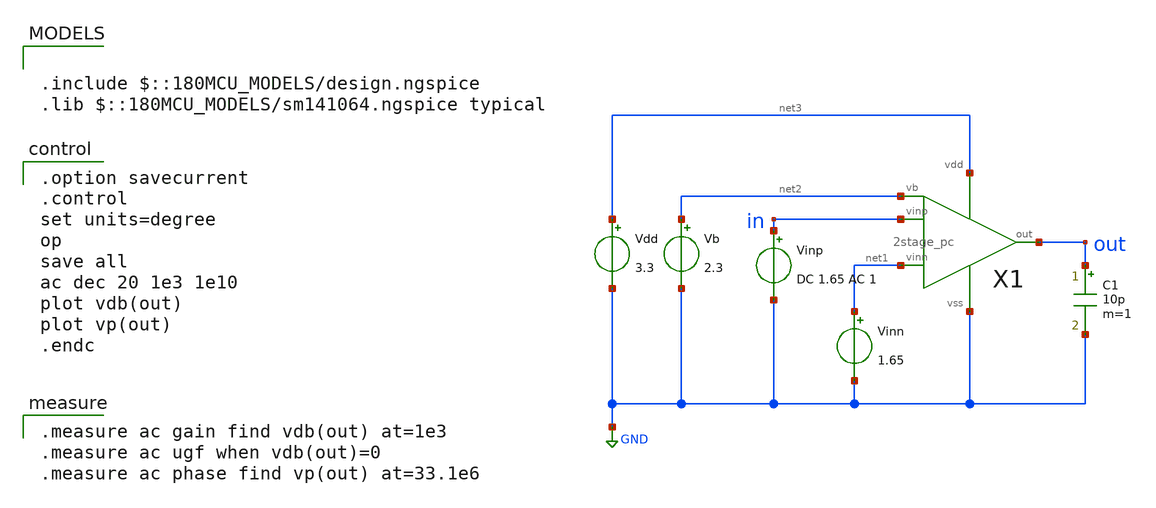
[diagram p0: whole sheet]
** sch_path: opamp/2stage_pc_ac.sch
**.subckt 2stage_pc_ac
Vdd net3 GND 3.3
Vb net2 GND 2.3
Vinn net1 GND 1.65
Vinp in GND DC 1.65 AC 1
C1 out GND 10p m=1
X1 in net1 net2 out net3 GND 2stage_pc
**** begin user architecture code

.include $::180MCU_MODELS/design.ngspice
.lib $::180MCU_MODELS/sm141064.ngspice typical


.option savecurrent
.control
set units=degree
op
save all
ac dec 20 1e3 1e10
plot vdb(out)
plot vp(out)
.endc


.measure ac gain find vdb(out) at=1e3
.measure ac ugf when vdb(out)=0
.measure ac phase find vp(out) at=33.1e6

**** end user architecture code
**.ends
.GLOBAL GND
.end
